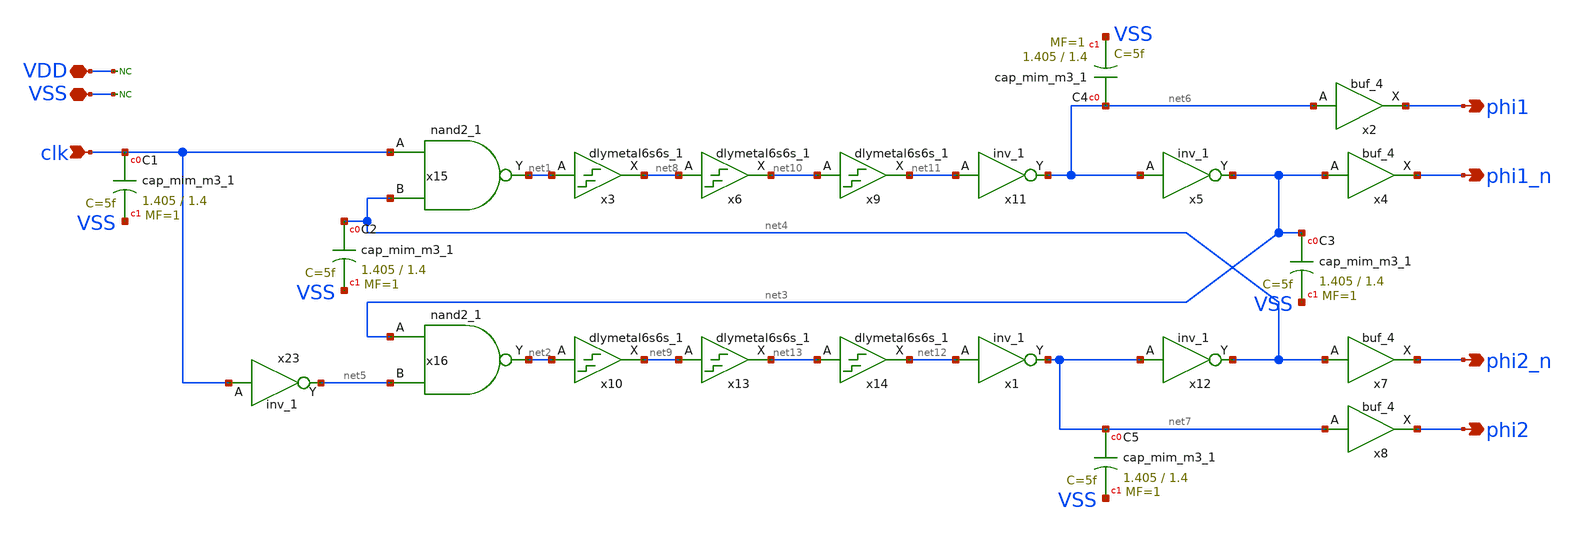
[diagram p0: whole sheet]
** sch_path: hgu/xschem/hgu_vgen_vcm_clkgen.sch
**.subckt hgu_vgen_vcm_clkgen VDD VSS phi2_n phi2 phi1 phi1_n clk
*.iopin VDD
*.iopin VSS
*.opin phi2_n
*.opin phi2
*.opin phi1
*.opin phi1_n
*.ipin clk
x23 clk VSS VSS VDD VDD net5 sky130_fd_sc_hd__inv_1
x2 net6 VSS VSS VDD VDD phi1 sky130_fd_sc_hd__buf_4
x5 net6 VSS VSS VDD VDD net3 sky130_fd_sc_hd__inv_1
x11 net11 VSS VSS VDD VDD net6 sky130_fd_sc_hd__inv_1
x12 net7 VSS VSS VDD VDD net4 sky130_fd_sc_hd__inv_1
x4 net3 VSS VSS VDD VDD phi1_n sky130_fd_sc_hd__buf_4
x7 net4 VSS VSS VDD VDD phi2_n sky130_fd_sc_hd__buf_4
x8 net7 VSS VSS VDD VDD phi2 sky130_fd_sc_hd__buf_4
x3 net1 VSS VSS VDD VDD net8 sky130_fd_sc_hd__dlymetal6s6s_1
x10 net2 VSS VSS VDD VDD net9 sky130_fd_sc_hd__dlymetal6s6s_1
x6 net8 VSS VSS VDD VDD net10 sky130_fd_sc_hd__dlymetal6s6s_1
x13 net9 VSS VSS VDD VDD net13 sky130_fd_sc_hd__dlymetal6s6s_1
x1 net12 VSS VSS VDD VDD net7 sky130_fd_sc_hd__inv_1
x9 net10 VSS VSS VDD VDD net11 sky130_fd_sc_hd__dlymetal6s6s_1
x14 net13 VSS VSS VDD VDD net12 sky130_fd_sc_hd__dlymetal6s6s_1
x15 clk net4 VSS VSS VDD VDD net1 sky130_fd_sc_hd__nand2_1
x16 net3 net5 VSS VSS VDD VDD net2 sky130_fd_sc_hd__nand2_1
* noconn VDD
* noconn VSS
XC1 clk VSS sky130_fd_pr__cap_mim_m3_1 W=1.405 L=1.4 MF=1 m=1
XC2 net4 VSS sky130_fd_pr__cap_mim_m3_1 W=1.405 L=1.4 MF=1 m=1
XC3 net3 VSS sky130_fd_pr__cap_mim_m3_1 W=1.405 L=1.4 MF=1 m=1
XC4 net6 VSS sky130_fd_pr__cap_mim_m3_1 W=1.405 L=1.4 MF=1 m=1
XC5 net7 VSS sky130_fd_pr__cap_mim_m3_1 W=1.405 L=1.4 MF=1 m=1
**.ends
.end
